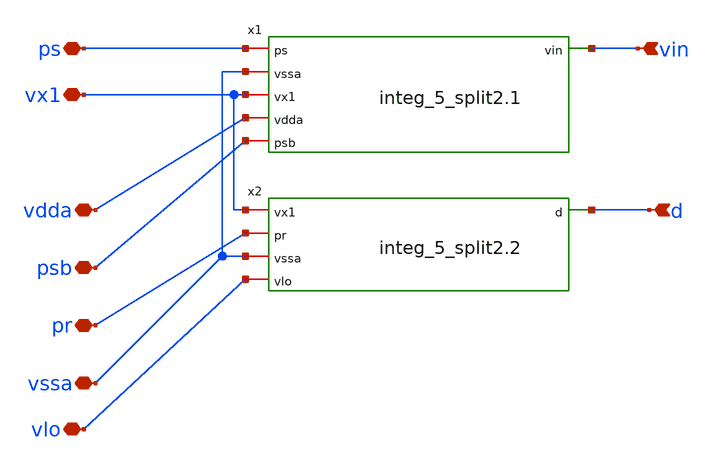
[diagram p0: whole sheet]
** sch_path: 5_Design/4_Layout/Team 5/splitUpSimulationsAndSchematics/integ_5_split2.sch
**.subckt integ_5_split2 d vlo vin pr psb ps vx1 vssa vdda
*.ipin d
*.iopin vlo
*.ipin vin
*.iopin pr
*.iopin psb
*.iopin ps
*.iopin vx1
*.iopin vssa
*.iopin vdda
x1 ps vssa vx1 vin vdda psb integ_5_split2.1
x2 vx1 pr vssa d vlo integ_5_split2.2
**.ends
.end
